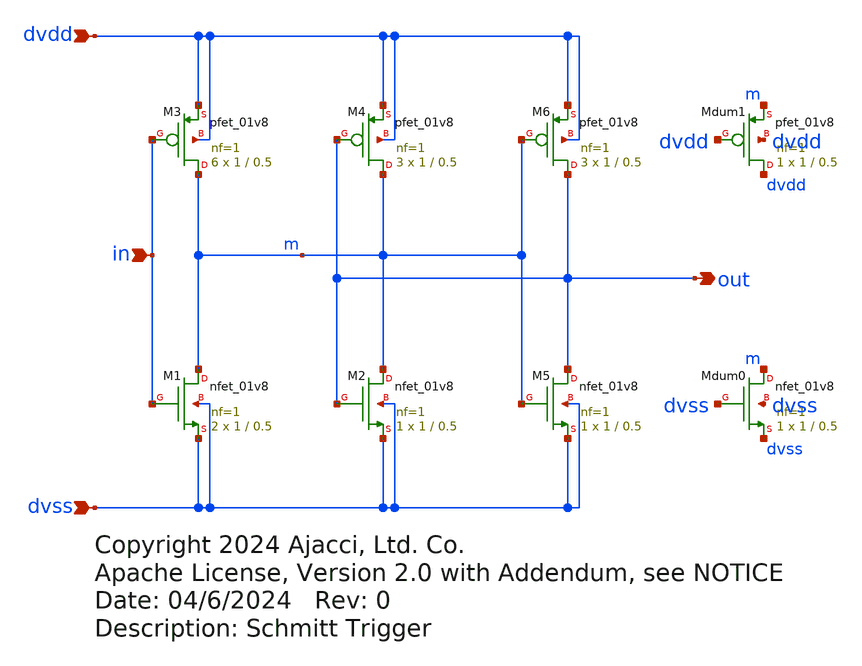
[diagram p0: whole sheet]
** sch_path: xschem/schmitt_trigger.sch
* Copyright 2024 Ajacci, Ltd. Co.
* Apache License, Version 2.0 with Addendum, see NOTICE
**.subckt schmitt_trigger dvdd dvss out in
*.ipin dvdd
*.ipin dvss
*.opin out
*.ipin in
XM1 m in dvss dvss sky130_fd_pr__nfet_01v8 L=0.5 W=1 nf=1 ad='int((nf+1)/2) * W/nf * 0.29' as='int((nf+2)/2) * W/nf * 0.29'
+ pd='2*int((nf+1)/2) * (W/nf + 0.29)' ps='2*int((nf+2)/2) * (W/nf + 0.29)' nrd='0.29 / W' nrs='0.29 / W'
+ sa=0 sb=0 sd=0 mult=2 m=2
XM3 m in dvdd dvdd sky130_fd_pr__pfet_01v8 L=0.5 W=1 nf=1 ad='int((nf+1)/2) * W/nf * 0.29' as='int((nf+2)/2) * W/nf * 0.29'
+ pd='2*int((nf+1)/2) * (W/nf + 0.29)' ps='2*int((nf+2)/2) * (W/nf + 0.29)' nrd='0.29 / W' nrs='0.29 / W'
+ sa=0 sb=0 sd=0 mult=6 m=6
XM2 m out dvss dvss sky130_fd_pr__nfet_01v8 L=0.5 W=1 nf=1 ad='int((nf+1)/2) * W/nf * 0.29' as='int((nf+2)/2) * W/nf * 0.29'
+ pd='2*int((nf+1)/2) * (W/nf + 0.29)' ps='2*int((nf+2)/2) * (W/nf + 0.29)' nrd='0.29 / W' nrs='0.29 / W'
+ sa=0 sb=0 sd=0 mult=1 m=1
XM4 m out dvdd dvdd sky130_fd_pr__pfet_01v8 L=0.5 W=1 nf=1 ad='int((nf+1)/2) * W/nf * 0.29' as='int((nf+2)/2) * W/nf * 0.29'
+ pd='2*int((nf+1)/2) * (W/nf + 0.29)' ps='2*int((nf+2)/2) * (W/nf + 0.29)' nrd='0.29 / W' nrs='0.29 / W'
+ sa=0 sb=0 sd=0 mult=3 m=3
XM5 out m dvss dvss sky130_fd_pr__nfet_01v8 L=0.5 W=1 nf=1 ad='int((nf+1)/2) * W/nf * 0.29' as='int((nf+2)/2) * W/nf * 0.29'
+ pd='2*int((nf+1)/2) * (W/nf + 0.29)' ps='2*int((nf+2)/2) * (W/nf + 0.29)' nrd='0.29 / W' nrs='0.29 / W'
+ sa=0 sb=0 sd=0 mult=1 m=1
XM6 out m dvdd dvdd sky130_fd_pr__pfet_01v8 L=0.5 W=1 nf=1 ad='int((nf+1)/2) * W/nf * 0.29' as='int((nf+2)/2) * W/nf * 0.29'
+ pd='2*int((nf+1)/2) * (W/nf + 0.29)' ps='2*int((nf+2)/2) * (W/nf + 0.29)' nrd='0.29 / W' nrs='0.29 / W'
+ sa=0 sb=0 sd=0 mult=3 m=3
XMdum0 m dvss dvss dvss sky130_fd_pr__nfet_01v8 L=0.5 W=1 nf=1 ad='int((nf+1)/2) * W/nf * 0.29' as='int((nf+2)/2) * W/nf * 0.29'
+ pd='2*int((nf+1)/2) * (W/nf + 0.29)' ps='2*int((nf+2)/2) * (W/nf + 0.29)' nrd='0.29 / W' nrs='0.29 / W'
+ sa=0 sb=0 sd=0 mult=1 m=1
XMdum1 dvdd dvdd m dvdd sky130_fd_pr__pfet_01v8 L=0.5 W=1 nf=1 ad='int((nf+1)/2) * W/nf * 0.29' as='int((nf+2)/2) * W/nf * 0.29'
+ pd='2*int((nf+1)/2) * (W/nf + 0.29)' ps='2*int((nf+2)/2) * (W/nf + 0.29)' nrd='0.29 / W' nrs='0.29 / W'
+ sa=0 sb=0 sd=0 mult=1 m=1
**.ends
.end
